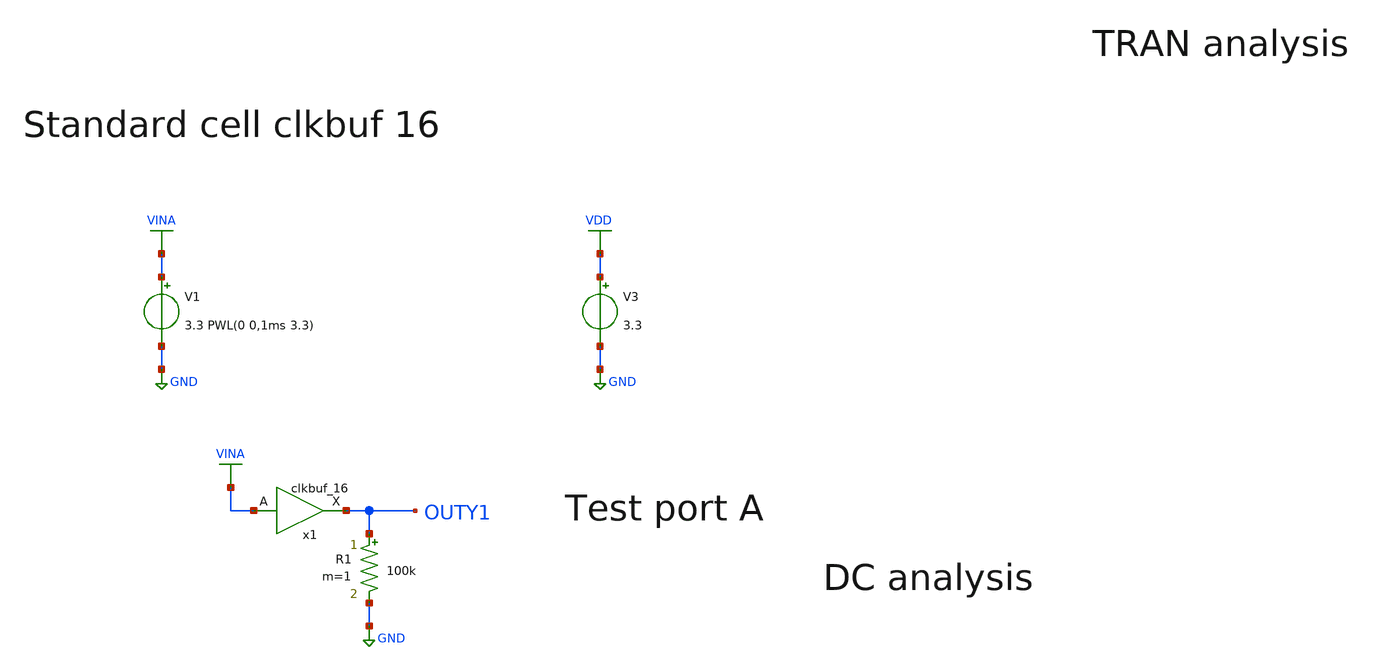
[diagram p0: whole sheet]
** sch_path: designs/libs/tb_analog/tb_std_clkbuf/tb_std_clkbuf.sch
* Copyright 2022 GlobalFoundries PDK Authors
* Licensed under the Apache License, Version 2.0 (the "License");
* you may not use this file except in compliance with the License.
* You may obtain a copy of the License at
* https://www.apache.org/licenses/LICENSE-2.0
* Unless required by applicable law or agreed to in writing, software
* distributed under the License is distributed on an "AS IS" BASIS,
* WITHOUT WARRANTIES OR CONDITIONS OF ANY KIND, either express or implied.
* See the License for the specific language governing permissions and
* limitations under the License.
**.subckt tb_std_clkbuf
V1 VINA GND 3.3 PWL(0 0,1ms 3.3)
V3 VDD GND 3.3
R1 OUTY1 GND 100k m=1
x1 VINA OUTY1 VDD VDD GND GND gf180mcu_fd_sc_mcu7t5v0__clkbuf_16
**** begin user architecture code


.control
save all
save currents
* DC analysis
dc v1 0 3.3 0.1
write tb_std_clkbuf_dc.raw

* TRANS analysis
tran 1u 2m
write tb_std_clkbuf_tran.raw
.endc



.include $::180MCU_MODELS/design.ngspice
.lib $::180MCU_MODELS/sm141064.ngspice typical
.include /foss/pdks/gf180mcuD/libs.ref/gf180mcu_fd_sc_mcu7t5v0/spice/gf180mcu_fd_sc_mcu7t5v0.spice


**** end user architecture code
**.ends
.GLOBAL VDD
.GLOBAL GND
.GLOBAL VINA
.end
